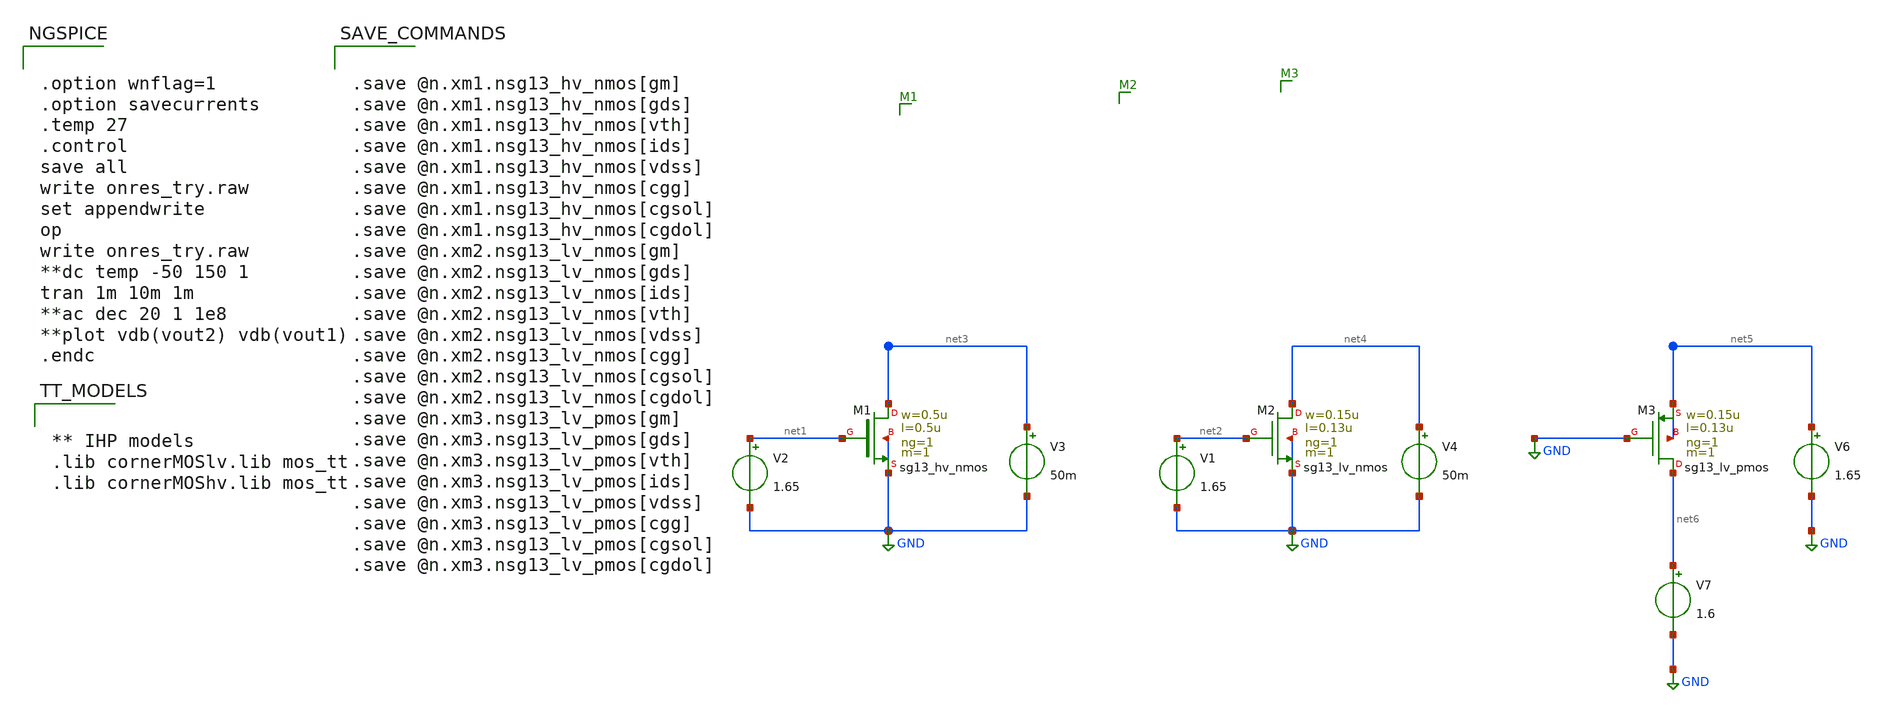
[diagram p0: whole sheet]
** sch_path: Design Files/RAMP/onres_try.sch
**.subckt onres_try
XM1 net3 net1 GND GND sg13_hv_nmos w=0.5u l=0.5u ng=1 m=1 mm_ok=1
XM2 net4 net2 GND GND sg13_lv_nmos w=0.15u l=0.13u ng=1 m=1 mm_ok=1
V2 net1 GND 1.65
V1 net2 GND 1.65
V3 net3 GND 50m
V4 net4 GND 50m
V6 net5 GND 1.65
XM3 net6 GND net5 net5 sg13_lv_pmos w=0.15u l=0.13u ng=1 m=1 mm_ok=1
V7 net6 GND 1.6
**** begin user architecture code


.option wnflag=1
.option savecurrents
.temp 27
.control
save all
write onres_try.raw
set appendwrite
op
write onres_try.raw
**dc temp -50 150 1
tran 1m 10m 1m
**ac dec 20 1 1e8
**plot vdb(vout2) vdb(vout1)
.endc




** IHP models
.lib cornerMOSlv.lib mos_tt
.lib cornerMOShv.lib mos_tt




.save @n.xm1.nsg13_hv_nmos[gm]
.save @n.xm1.nsg13_hv_nmos[gds]
.save @n.xm1.nsg13_hv_nmos[vth]
.save @n.xm1.nsg13_hv_nmos[ids]
.save @n.xm1.nsg13_hv_nmos[vdss]
.save @n.xm1.nsg13_hv_nmos[cgg]
.save @n.xm1.nsg13_hv_nmos[cgsol]
.save @n.xm1.nsg13_hv_nmos[cgdol]
.save @n.xm2.nsg13_lv_nmos[gm]
.save @n.xm2.nsg13_lv_nmos[gds]
.save @n.xm2.nsg13_lv_nmos[ids]
.save @n.xm2.nsg13_lv_nmos[vth]
.save @n.xm2.nsg13_lv_nmos[vdss]
.save @n.xm2.nsg13_lv_nmos[cgg]
.save @n.xm2.nsg13_lv_nmos[cgsol]
.save @n.xm2.nsg13_lv_nmos[cgdol]
.save @n.xm3.nsg13_lv_pmos[gm]
.save @n.xm3.nsg13_lv_pmos[gds]
.save @n.xm3.nsg13_lv_pmos[vth]
.save @n.xm3.nsg13_lv_pmos[ids]
.save @n.xm3.nsg13_lv_pmos[vdss]
.save @n.xm3.nsg13_lv_pmos[cgg]
.save @n.xm3.nsg13_lv_pmos[cgsol]
.save @n.xm3.nsg13_lv_pmos[cgdol]


**** end user architecture code
**.ends
.GLOBAL GND
.end
